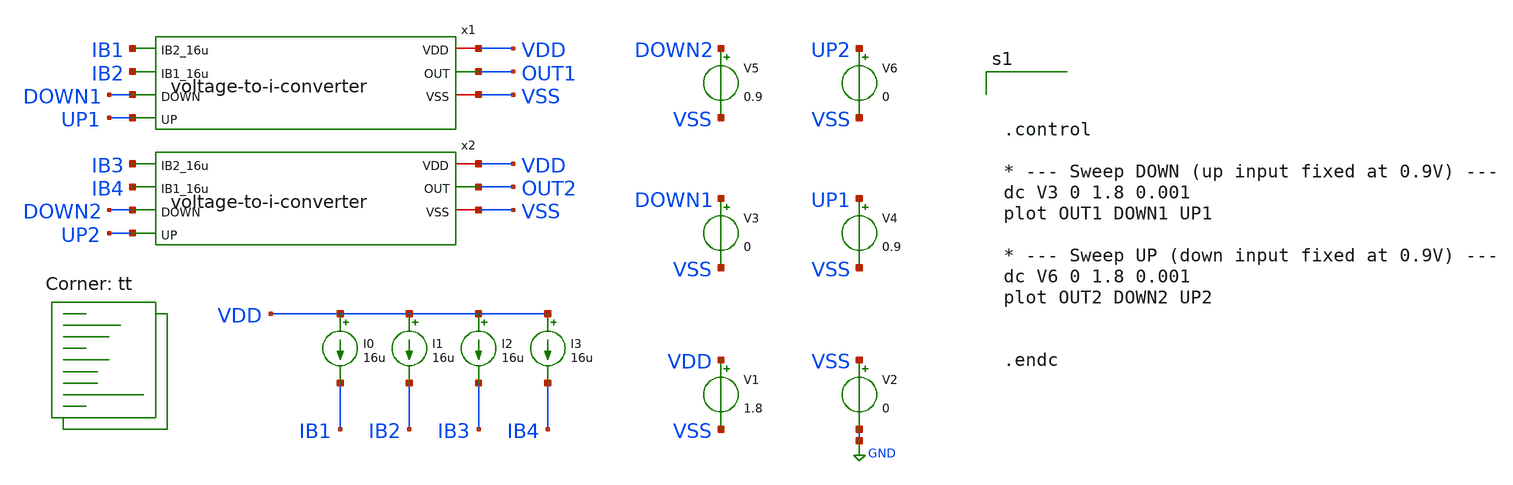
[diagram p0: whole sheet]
** sch_path: v-i-converter/tb_dc.sch
**.subckt tb_dc
V1 VDD VSS 1.8
V2 VSS GND 0
V3 DOWN1 VSS 0
V4 UP1 VSS 0.9
x1 VDD IB1 IB2 OUT1 DOWN1 UP1 VSS voltage-to-i-converter
x2 VDD IB3 IB4 OUT2 DOWN2 UP2 VSS voltage-to-i-converter
V5 DOWN2 VSS 0.9
V6 UP2 VSS 0
I0 VDD IB1 16u
I1 VDD IB2 16u
I2 VDD IB3 16u
I3 VDD IB4 16u
**** begin user architecture code
.lib $::SKYWATER_MODELS/sky130.lib.spice tt



.control

* --- Sweep DOWN (up input fixed at 0.9V) ---
dc V3 0 1.8 0.001
plot OUT1 DOWN1 UP1

* --- Sweep UP (down input fixed at 0.9V) ---
dc V6 0 1.8 0.001
plot OUT2 DOWN2 UP2


.endc


**** end user architecture code
**.ends

* expanding   symbol:  /foss/designs/afe-icdec-teknofest-2026/CTLE/voltage-to-i-converter.sym # of
*+ pins=7
** sym_path: CTLE/voltage-to-i-converter.sym
** sch_path: CTLE/voltage-to-i-converter.sch
.subckt voltage-to-i-converter VDD IB2_16u IB1_16u OUT DOWN UP VSS
*.iopin VDD
*.iopin VSS
*.opin OUT
*.ipin IB2_16u
*.ipin UP
*.ipin DOWN
*.ipin IB1_16u
XM1 net4 net4 VDD VDD sky130_fd_pr__pfet_01v8 L=0.6 W=75 nf=1 ad='int((nf+1)/2) * W/nf * 0.29' as='int((nf+2)/2) * W/nf * 0.29'
+ pd='2*int((nf+1)/2) * (W/nf + 0.29)' ps='2*int((nf+2)/2) * (W/nf + 0.29)' nrd='0.29 / W' nrs='0.29 / W'
+ sa=0 sb=0 sd=0 mult=1 m=1
XM2 net6 net6 VDD VDD sky130_fd_pr__pfet_01v8 L=0.6 W=75 nf=1 ad='int((nf+1)/2) * W/nf * 0.29' as='int((nf+2)/2) * W/nf * 0.29'
+ pd='2*int((nf+1)/2) * (W/nf + 0.29)' ps='2*int((nf+2)/2) * (W/nf + 0.29)' nrd='0.29 / W' nrs='0.29 / W'
+ sa=0 sb=0 sd=0 mult=1 m=1
XM5 net1 IB1_16u VSS VSS sky130_fd_pr__nfet_01v8 L=1.5 W=25 nf=1 ad='int((nf+1)/2) * W/nf * 0.29' as='int((nf+2)/2) * W/nf * 0.29'
+ pd='2*int((nf+1)/2) * (W/nf + 0.29)' ps='2*int((nf+2)/2) * (W/nf + 0.29)' nrd='0.29 / W' nrs='0.29 / W'
+ sa=0 sb=0 sd=0 mult=1 m=1
XM6 IB1_16u IB1_16u VSS VSS sky130_fd_pr__nfet_01v8 L=1.5 W=25 nf=1 ad='int((nf+1)/2) * W/nf * 0.29'
+ as='int((nf+2)/2) * W/nf * 0.29' pd='2*int((nf+1)/2) * (W/nf + 0.29)' ps='2*int((nf+2)/2) * (W/nf + 0.29)'
+ nrd='0.29 / W' nrs='0.29 / W' sa=0 sb=0 sd=0 mult=1 m=1
XM7 net5 net5 VDD VDD sky130_fd_pr__pfet_01v8 L=0.6 W=75 nf=1 ad='int((nf+1)/2) * W/nf * 0.29' as='int((nf+2)/2) * W/nf * 0.29'
+ pd='2*int((nf+1)/2) * (W/nf + 0.29)' ps='2*int((nf+2)/2) * (W/nf + 0.29)' nrd='0.29 / W' nrs='0.29 / W'
+ sa=0 sb=0 sd=0 mult=1 m=1
XM8 net7 net7 VDD VDD sky130_fd_pr__pfet_01v8 L=0.6 W=75 nf=1 ad='int((nf+1)/2) * W/nf * 0.29' as='int((nf+2)/2) * W/nf * 0.29'
+ pd='2*int((nf+1)/2) * (W/nf + 0.29)' ps='2*int((nf+2)/2) * (W/nf + 0.29)' nrd='0.29 / W' nrs='0.29 / W'
+ sa=0 sb=0 sd=0 mult=1 m=1
XM11 net2 IB2_16u VSS VSS sky130_fd_pr__nfet_01v8 L=1.5 W=25 nf=1 ad='int((nf+1)/2) * W/nf * 0.29' as='int((nf+2)/2) * W/nf * 0.29'
+ pd='2*int((nf+1)/2) * (W/nf + 0.29)' ps='2*int((nf+2)/2) * (W/nf + 0.29)' nrd='0.29 / W' nrs='0.29 / W'
+ sa=0 sb=0 sd=0 mult=1 m=1
XM12 IB2_16u IB2_16u VSS VSS sky130_fd_pr__nfet_01v8 L=1.5 W=25 nf=1 ad='int((nf+1)/2) * W/nf * 0.29'
+ as='int((nf+2)/2) * W/nf * 0.29' pd='2*int((nf+1)/2) * (W/nf + 0.29)' ps='2*int((nf+2)/2) * (W/nf + 0.29)'
+ nrd='0.29 / W' nrs='0.29 / W' sa=0 sb=0 sd=0 mult=1 m=1
XM13 OUT net7 VDD VDD sky130_fd_pr__pfet_01v8 L=0.6 W=75 nf=1 ad='int((nf+1)/2) * W/nf * 0.29' as='int((nf+2)/2) * W/nf * 0.29'
+ pd='2*int((nf+1)/2) * (W/nf + 0.29)' ps='2*int((nf+2)/2) * (W/nf + 0.29)' nrd='0.29 / W' nrs='0.29 / W'
+ sa=0 sb=0 sd=0 mult=1 m=1
XM14 net8 net6 VDD VDD sky130_fd_pr__pfet_01v8 L=0.6 W=75 nf=1 ad='int((nf+1)/2) * W/nf * 0.29' as='int((nf+2)/2) * W/nf * 0.29'
+ pd='2*int((nf+1)/2) * (W/nf + 0.29)' ps='2*int((nf+2)/2) * (W/nf + 0.29)' nrd='0.29 / W' nrs='0.29 / W'
+ sa=0 sb=0 sd=0 mult=1 m=1
XM15 net8 net8 VSS VSS sky130_fd_pr__nfet_01v8 L=1.5 W=25 nf=1 ad='int((nf+1)/2) * W/nf * 0.29' as='int((nf+2)/2) * W/nf * 0.29'
+ pd='2*int((nf+1)/2) * (W/nf + 0.29)' ps='2*int((nf+2)/2) * (W/nf + 0.29)' nrd='0.29 / W' nrs='0.29 / W'
+ sa=0 sb=0 sd=0 mult=1 m=1
XM16 OUT net8 VSS VSS sky130_fd_pr__nfet_01v8 L=1.5 W=25 nf=1 ad='int((nf+1)/2) * W/nf * 0.29' as='int((nf+2)/2) * W/nf * 0.29'
+ pd='2*int((nf+1)/2) * (W/nf + 0.29)' ps='2*int((nf+2)/2) * (W/nf + 0.29)' nrd='0.29 / W' nrs='0.29 / W'
+ sa=0 sb=0 sd=0 mult=1 m=1
XR1 DOWN net3 VSS sky130_fd_pr__res_high_po_0p35 L=50 mult=1 m=1
XR2 net3 UP VSS sky130_fd_pr__res_high_po_0p35 L=50 mult=1 m=1
XC1 OUT VSS sky130_fd_pr__cap_mim_m3_1 W=30 L=30 MF=4 m=4
XM3 net6 DOWN net1 VSS sky130_fd_pr__nfet_01v8 L=0.5 W=25 nf=1 ad='int((nf+1)/2) * W/nf * 0.29' as='int((nf+2)/2) * W/nf * 0.29'
+ pd='2*int((nf+1)/2) * (W/nf + 0.29)' ps='2*int((nf+2)/2) * (W/nf + 0.29)' nrd='0.29 / W' nrs='0.29 / W'
+ sa=0 sb=0 sd=0 mult=1 m=1
XM4 net4 net3 net1 VSS sky130_fd_pr__nfet_01v8 L=0.5 W=25 nf=1 ad='int((nf+1)/2) * W/nf * 0.29' as='int((nf+2)/2) * W/nf * 0.29'
+ pd='2*int((nf+1)/2) * (W/nf + 0.29)' ps='2*int((nf+2)/2) * (W/nf + 0.29)' nrd='0.29 / W' nrs='0.29 / W'
+ sa=0 sb=0 sd=0 mult=1 m=1
XM9 net5 net3 net2 VSS sky130_fd_pr__nfet_01v8 L=0.5 W=25 nf=1 ad='int((nf+1)/2) * W/nf * 0.29' as='int((nf+2)/2) * W/nf * 0.29'
+ pd='2*int((nf+1)/2) * (W/nf + 0.29)' ps='2*int((nf+2)/2) * (W/nf + 0.29)' nrd='0.29 / W' nrs='0.29 / W'
+ sa=0 sb=0 sd=0 mult=1 m=1
XM10 net7 UP net2 VSS sky130_fd_pr__nfet_01v8 L=0.5 W=25 nf=1 ad='int((nf+1)/2) * W/nf * 0.29' as='int((nf+2)/2) * W/nf * 0.29'
+ pd='2*int((nf+1)/2) * (W/nf + 0.29)' ps='2*int((nf+2)/2) * (W/nf + 0.29)' nrd='0.29 / W' nrs='0.29 / W'
+ sa=0 sb=0 sd=0 mult=1 m=1
.ends

.GLOBAL GND
.end
